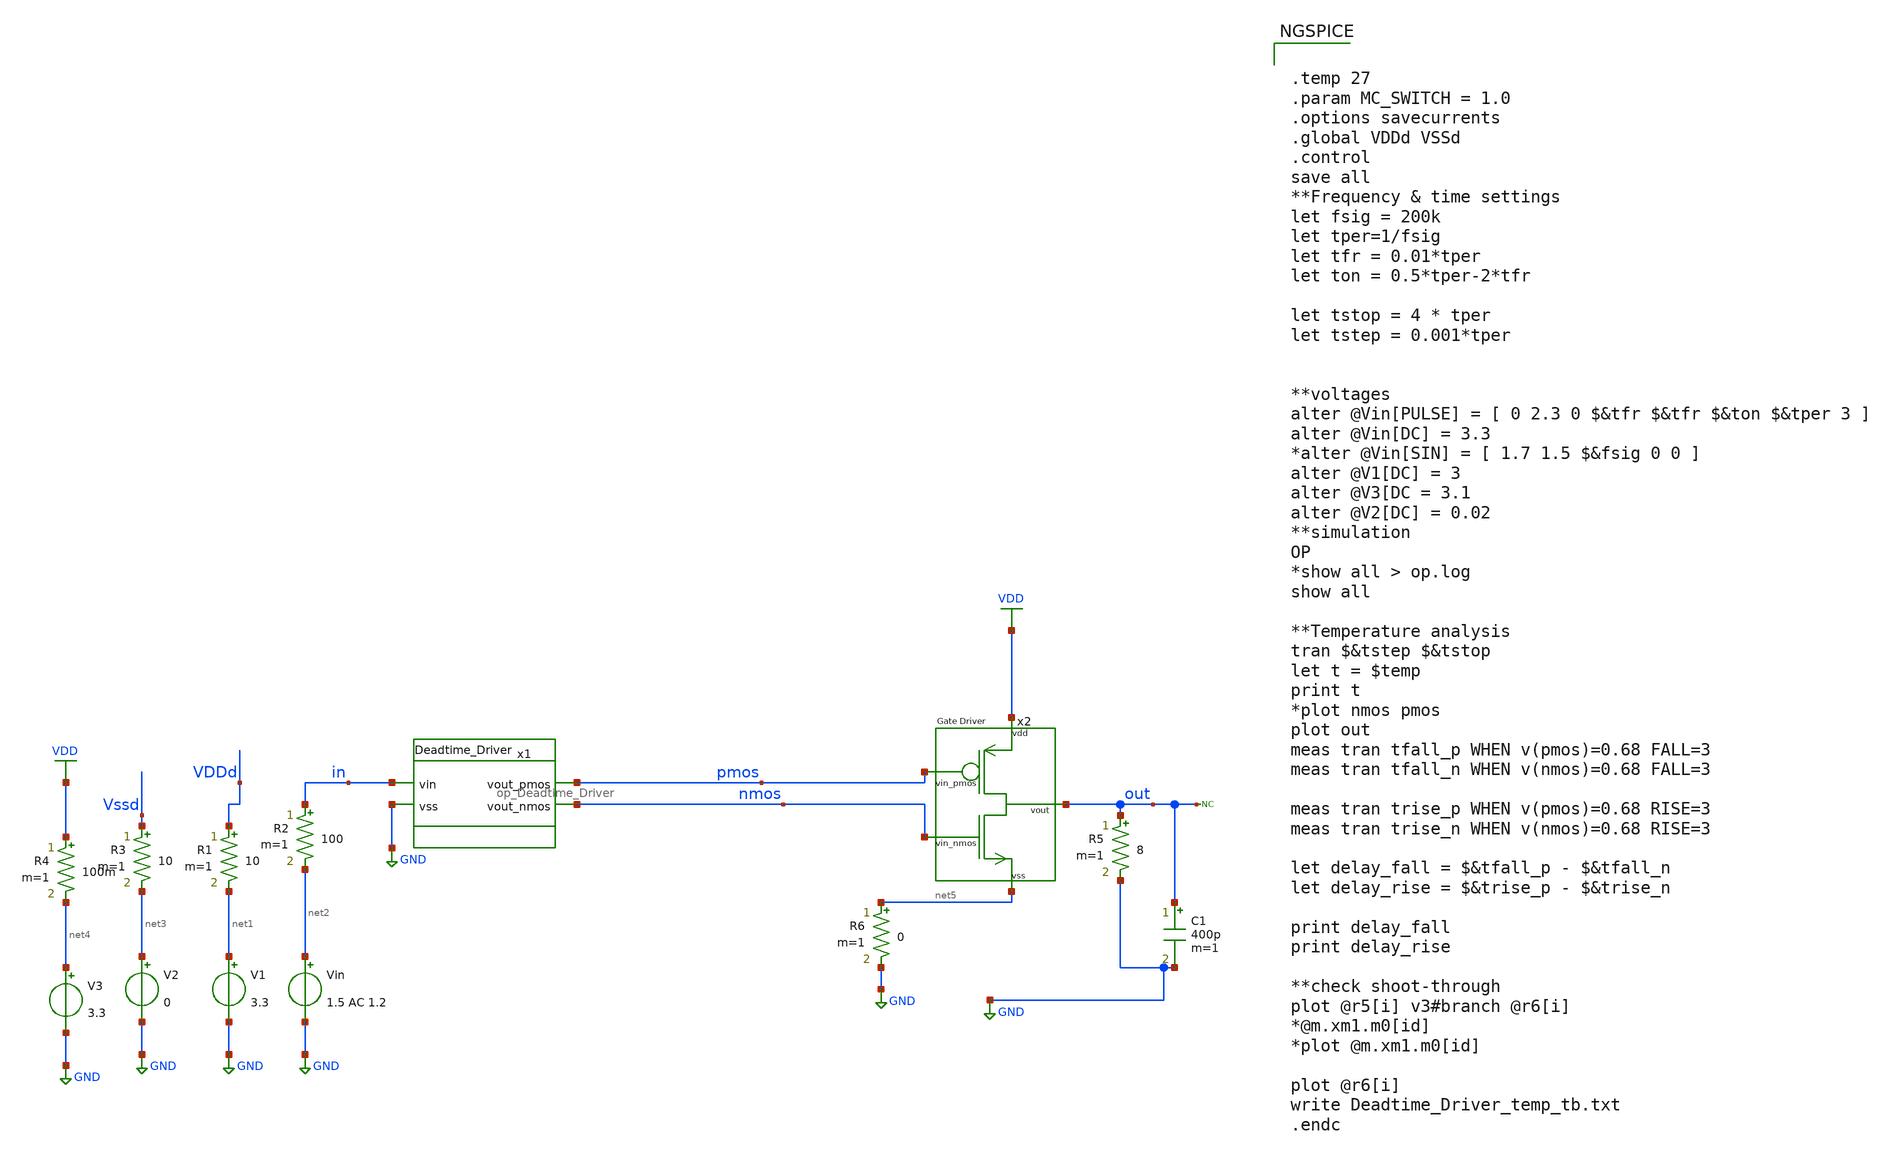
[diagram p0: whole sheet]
** sch_path: designs/libs/tb_analog/tb_op_Deadtime_Driver/tb_temp_deadtime_driver.sch
**.subckt tb_temp_deadtime_driver
V1 net1 GND 3.3
Vin net2 GND 1.5 AC 1.2
R1 VDDd net1 10 m=1
R2 in net2 100 m=1
V2 net3 GND 0
R3 Vssd net3 10 m=1
x1 pmos in nmos GND op_Deadtime_Driver
* noconn out
V3 net4 GND 3.3
R4 VDD net4 100m m=1
R5 out GND 8 m=1
C1 out GND 400p m=1
R6 net5 GND 0 m=1
x2 VDD pmos out nmos net5 Output_Stage
**** begin user architecture code

.include $::180MCU_MODELS/design.ngspice
.include /foss/pdks/gf180mcuD/libs.ref/gf180mcu_fd_sc_mcu9t5v0/spice/gf180mcu_fd_sc_mcu9t5v0.spice
.lib $::180MCU_MODELS/sm141064.ngspice typical
.lib $::180MCU_MODELS/sm141064.ngspice cap_mim
.lib $::180MCU_MODELS/sm141064.ngspice mimcap_typical



.temp 27
.param MC_SWITCH = 1.0
.options savecurrents
.global VDDd VSSd
.control
save all
**Frequency & time settings
let fsig = 200k
let tper=1/fsig
let tfr = 0.01*tper
let ton = 0.5*tper-2*tfr

let tstop = 4 * tper
let tstep = 0.001*tper


**voltages
alter @Vin[PULSE] = [ 0 2.3 0 $&tfr $&tfr $&ton $&tper 3 ]
alter @Vin[DC] = 3.3
*alter @Vin[SIN] = [ 1.7 1.5 $&fsig 0 0 ]
alter @V1[DC] = 3
alter @V3[DC = 3.1
alter @V2[DC] = 0.02
**simulation
OP
*show all > op.log
show all

**Temperature analysis
tran $&tstep $&tstop
let t = $temp
print t
*plot nmos pmos
plot out
meas tran tfall_p WHEN v(pmos)=0.68 FALL=3
meas tran tfall_n WHEN v(nmos)=0.68 FALL=3

meas tran trise_p WHEN v(pmos)=0.68 RISE=3
meas tran trise_n WHEN v(nmos)=0.68 RISE=3

let delay_fall = $&tfall_p - $&tfall_n
let delay_rise = $&trise_p - $&trise_n

print delay_fall
print delay_rise

**check shoot-through
plot @r5[i] v3#branch @r6[i]
*@m.xm1.m0[id]
*plot @m.xm1.m0[id]

plot @r6[i]
write Deadtime_Driver_temp_tb.txt
.endc


**** end user architecture code
**.ends
.GLOBAL GND
.GLOBAL VDD
.end
